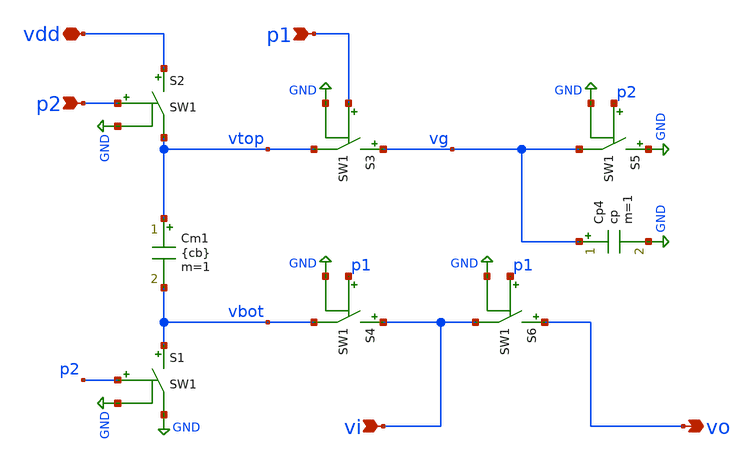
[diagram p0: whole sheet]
** sch_path: xschem/boot0.sch
**.subckt boot0 vi vo p2 p1 vdd
*.ipin vi
*.opin vo
*.ipin p2
*.ipin p1
*.iopin vdd
Cm1 vtop vbot {cb} m=1
S1 vbot GND p2 GND SW1
S2 vdd vtop p2 GND SW1
S3 vg vtop p1 GND SW1
S4 vi vbot p1 GND SW1
S5 GND vg p2 GND SW1
Cp4 vg GND cp m=1
S6 vo vi p1 GND SW1
**.ends
.GLOBAL GND
**** begin user architecture code
.MODEL SW1 SW   VT=0.6 VH=vh  RON=rsw ROFF=roff
**** end user architecture code
.end
